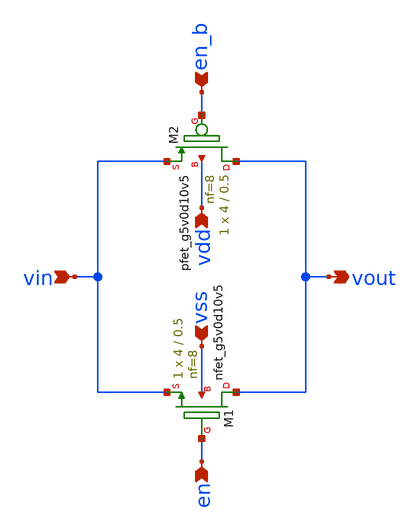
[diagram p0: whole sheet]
** sch_path: xschem/tg5v0.sch
**.subckt tg5v0 vin vout en en_b vdd vss
*.ipin vin
*.opin vout
*.ipin en
*.ipin en_b
*.ipin vdd
*.ipin vss
XM1 vout en vin vss sky130_fd_pr__nfet_g5v0d10v5 L=0.5 W=4 nf=8 ad='int((nf+1)/2) * W/nf * 0.29' as='int((nf+2)/2) * W/nf * 0.29'
+ pd='2*int((nf+1)/2) * (W/nf + 0.29)' ps='2*int((nf+2)/2) * (W/nf + 0.29)' nrd='0.29 / W' nrs='0.29 / W'
+ sa=0 sb=0 sd=0 mult=1 m=1
XM2 vout en_b vin vdd sky130_fd_pr__pfet_g5v0d10v5 L=0.5 W=4 nf=8 ad='int((nf+1)/2) * W/nf * 0.29' as='int((nf+2)/2) * W/nf * 0.29'
+ pd='2*int((nf+1)/2) * (W/nf + 0.29)' ps='2*int((nf+2)/2) * (W/nf + 0.29)' nrd='0.29 / W' nrs='0.29 / W'
+ sa=0 sb=0 sd=0 mult=1 m=1
**.ends
.end
